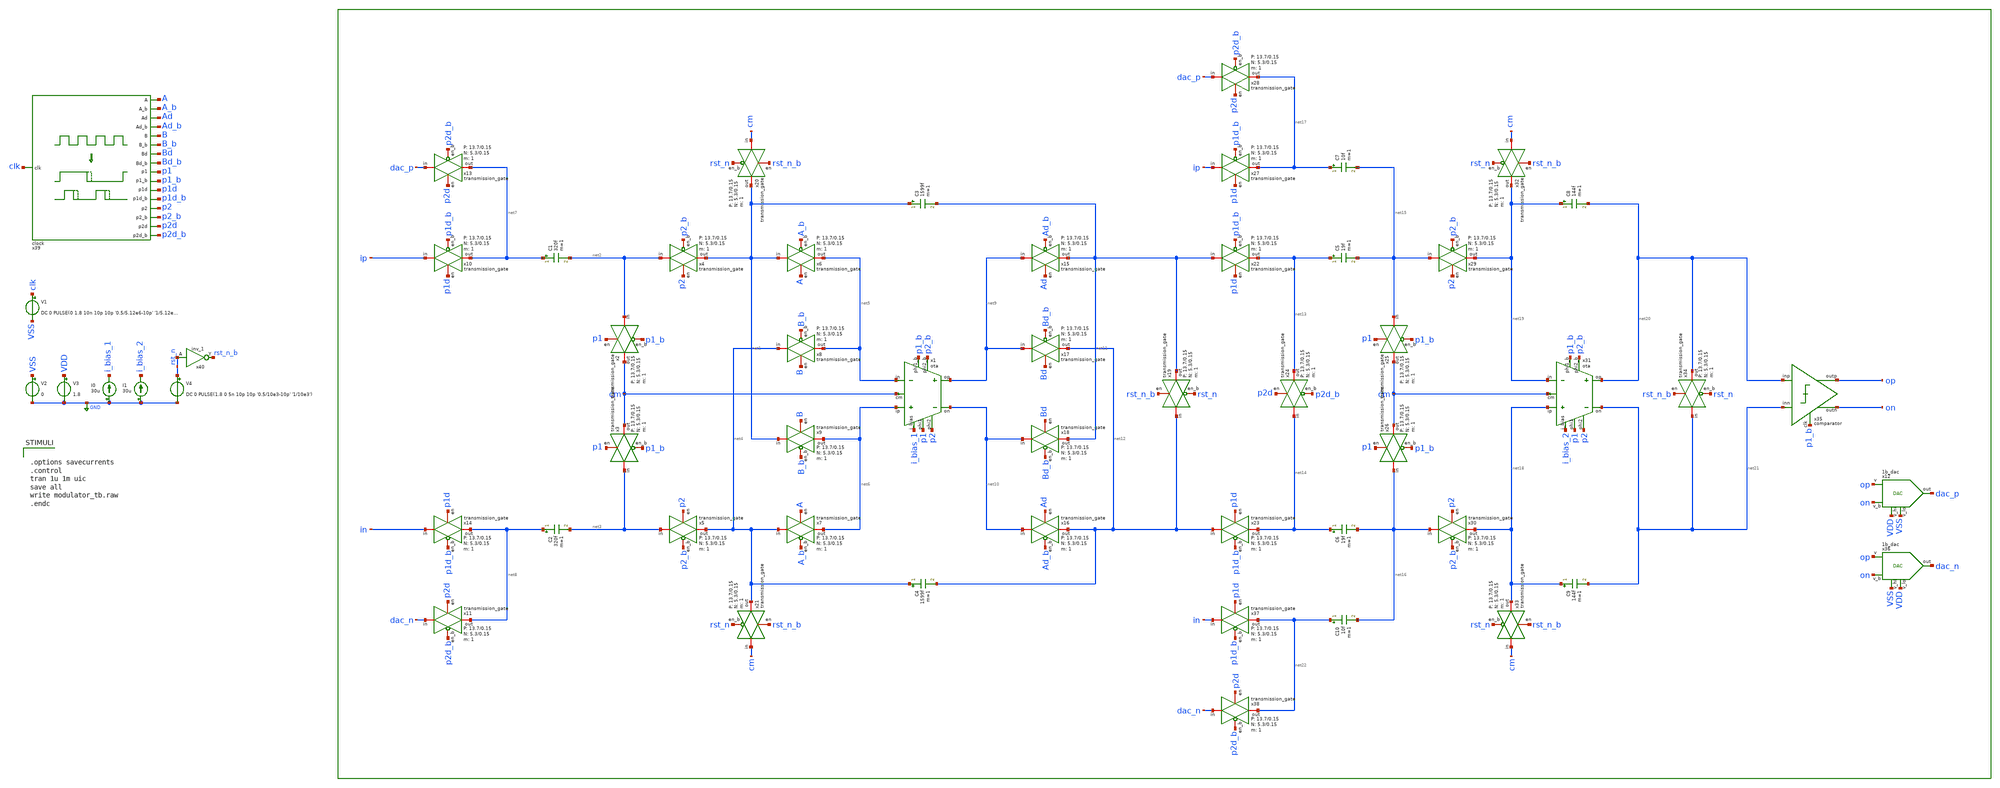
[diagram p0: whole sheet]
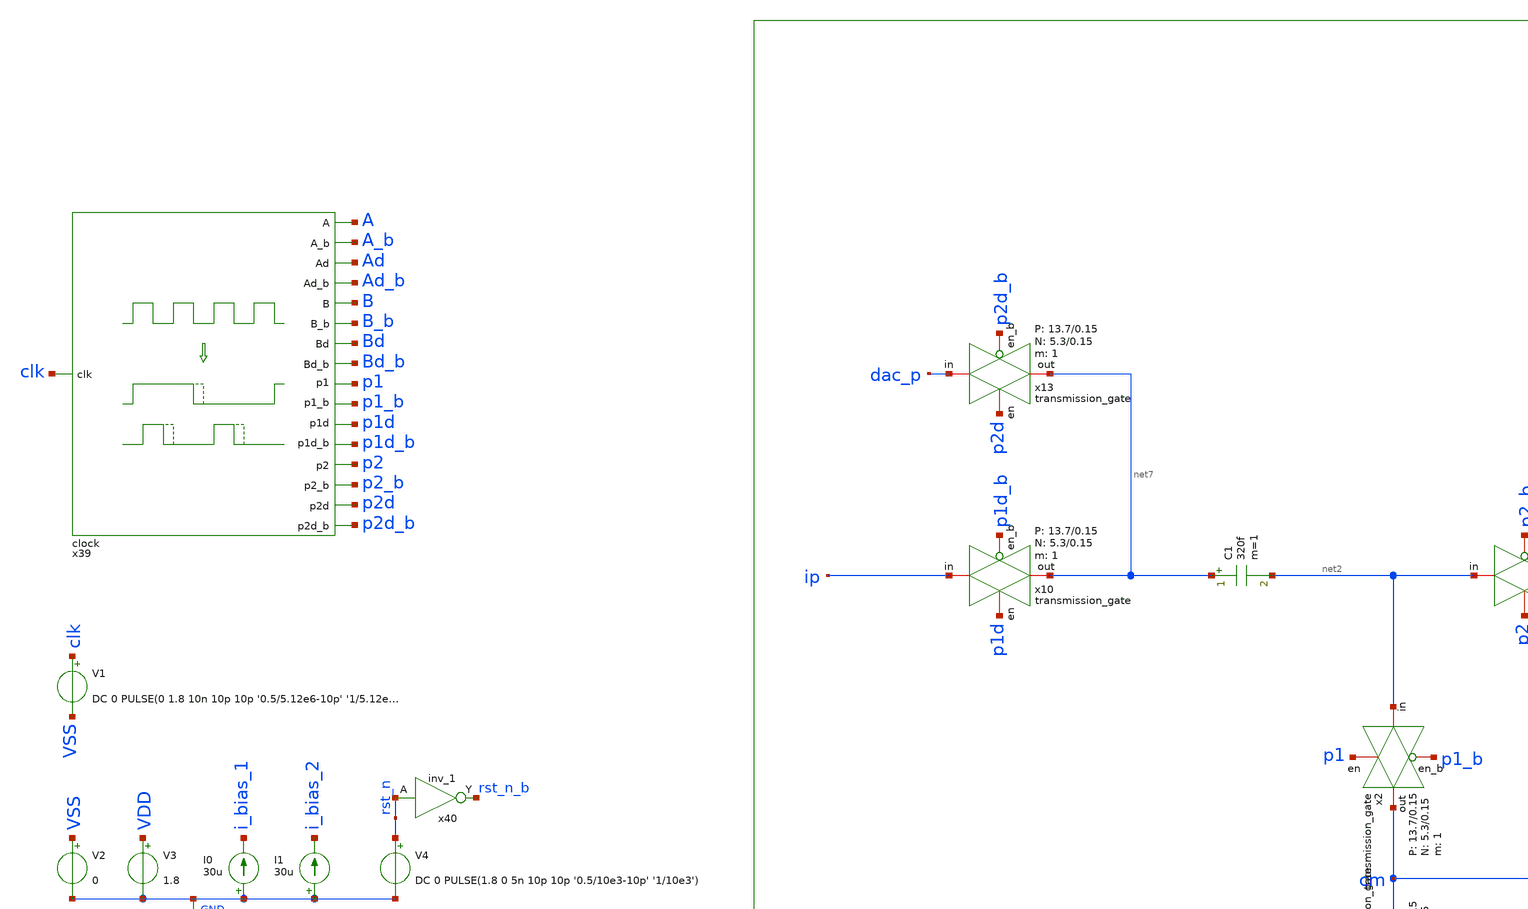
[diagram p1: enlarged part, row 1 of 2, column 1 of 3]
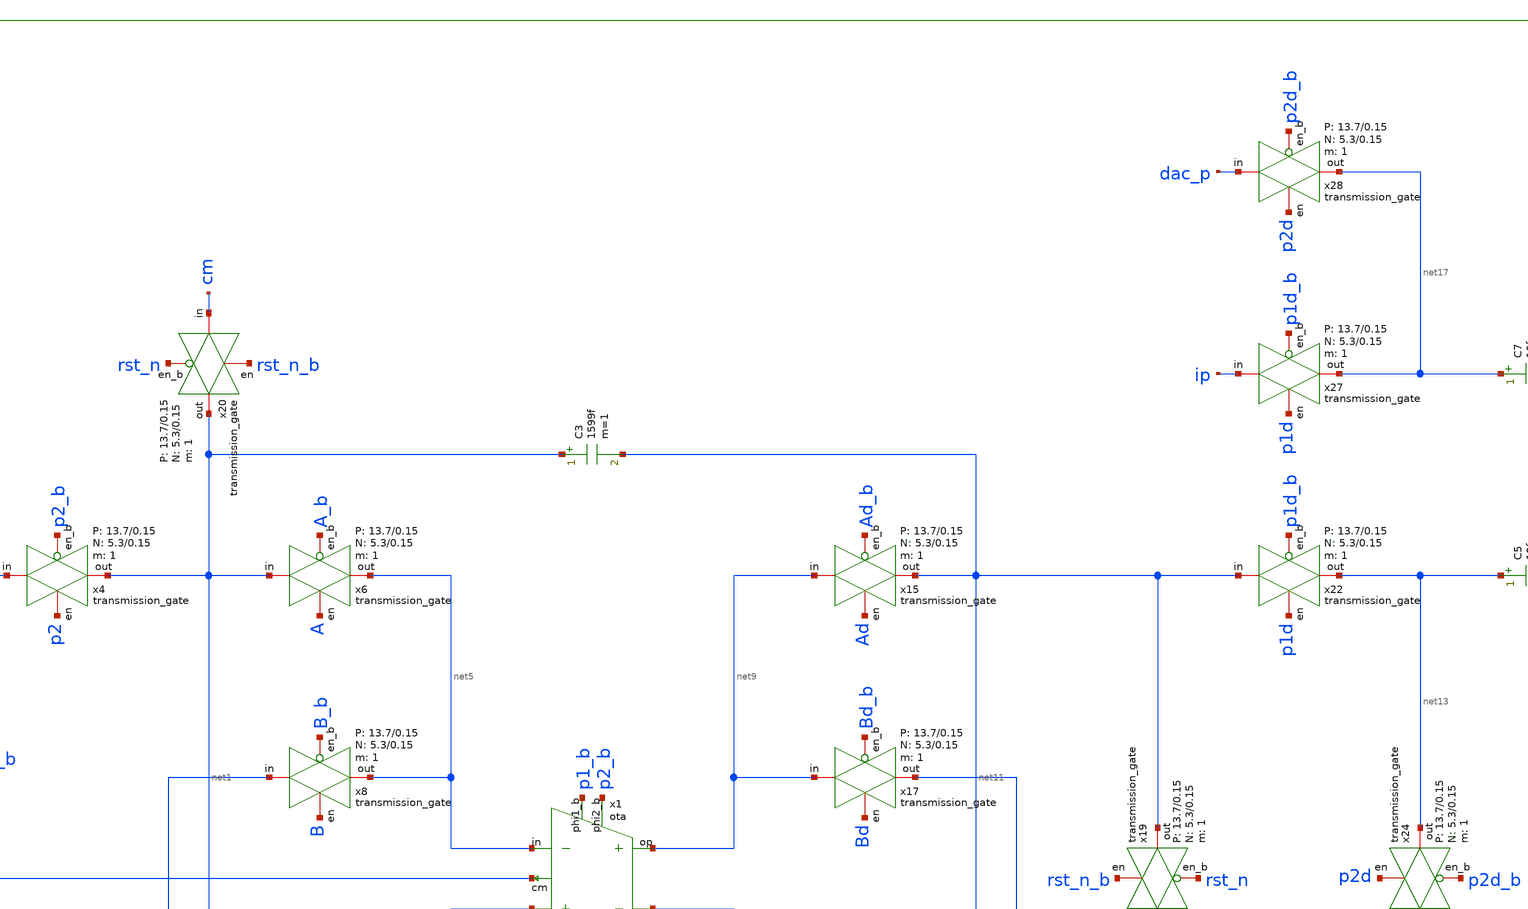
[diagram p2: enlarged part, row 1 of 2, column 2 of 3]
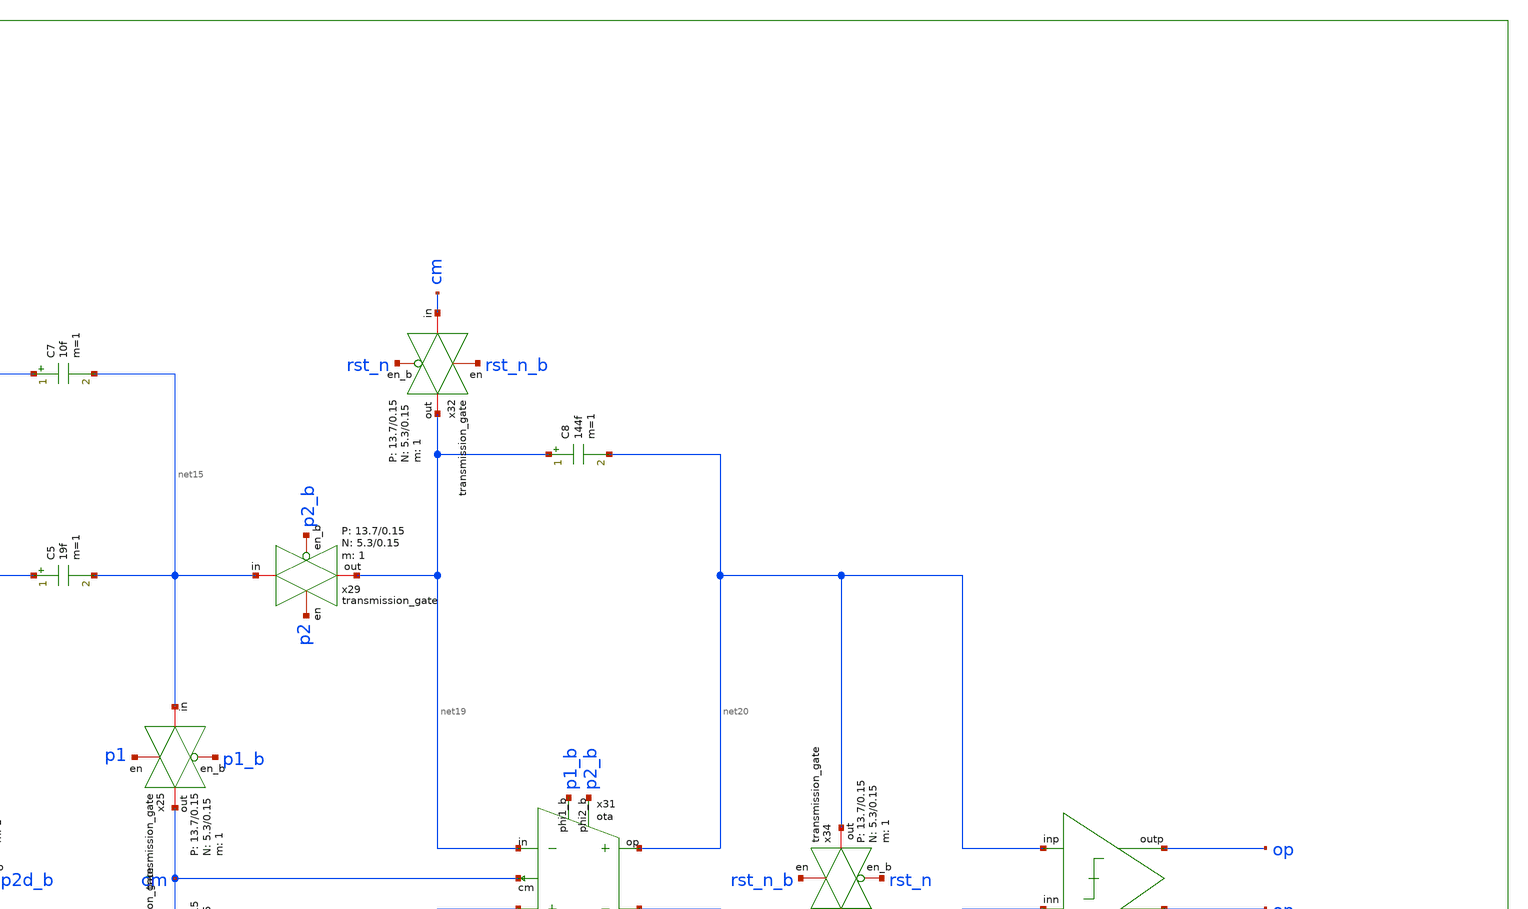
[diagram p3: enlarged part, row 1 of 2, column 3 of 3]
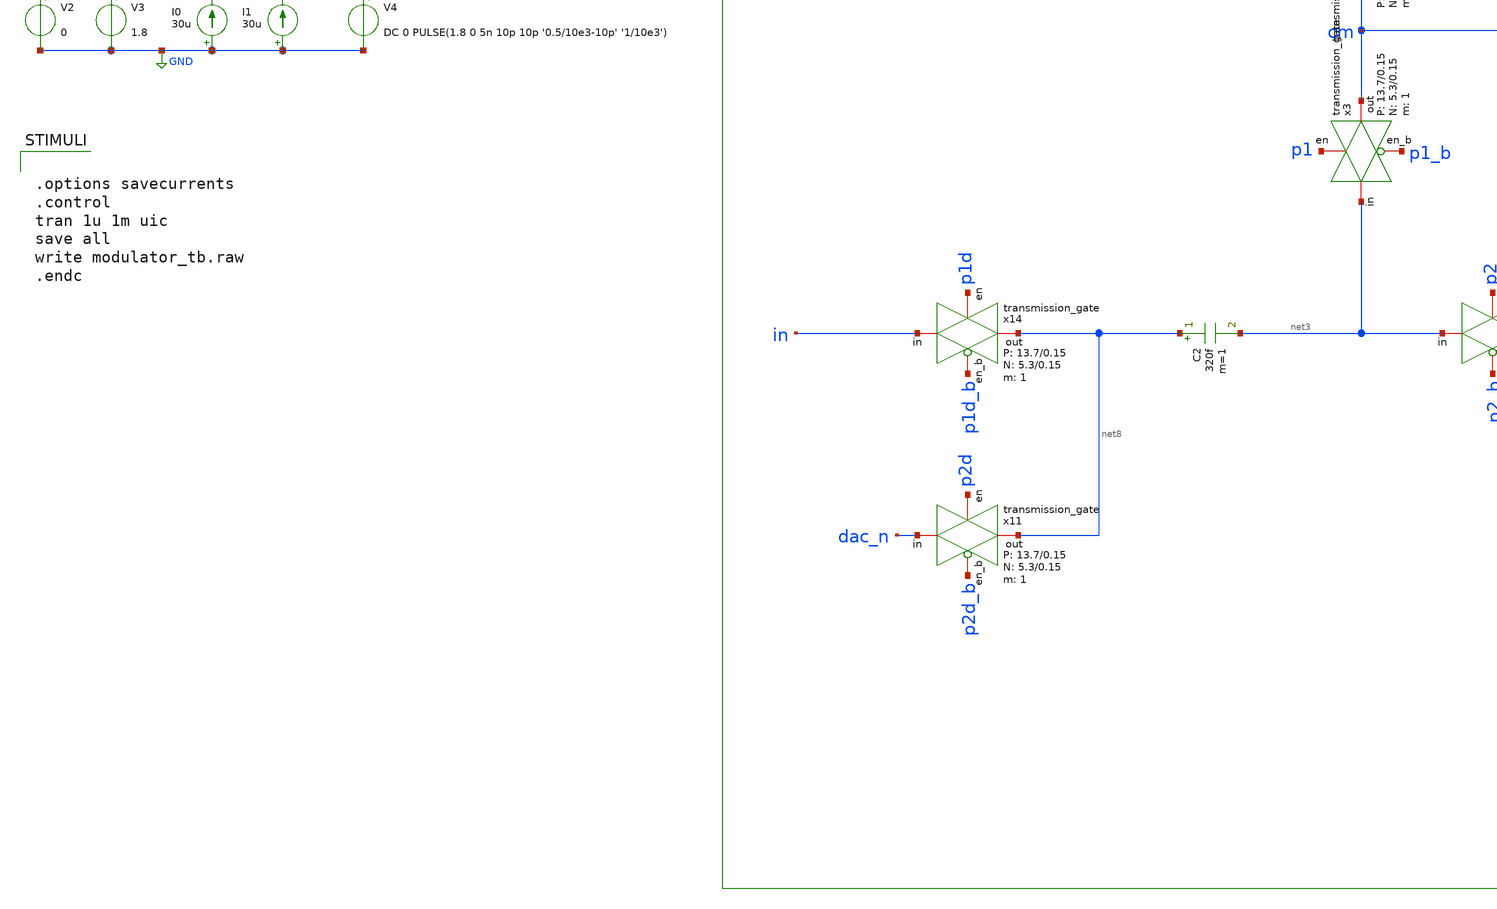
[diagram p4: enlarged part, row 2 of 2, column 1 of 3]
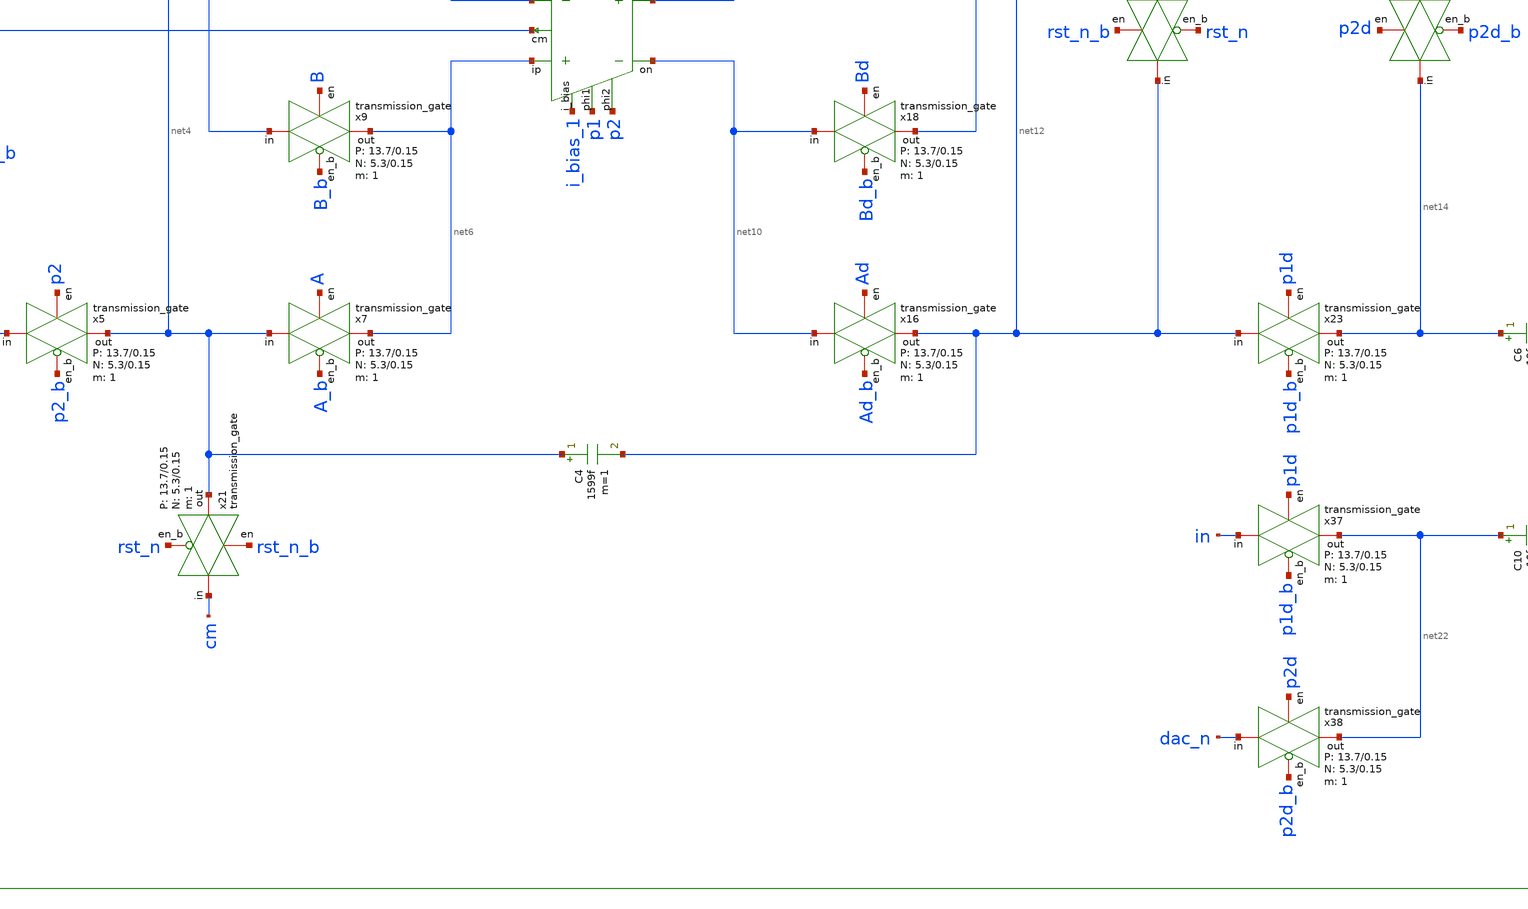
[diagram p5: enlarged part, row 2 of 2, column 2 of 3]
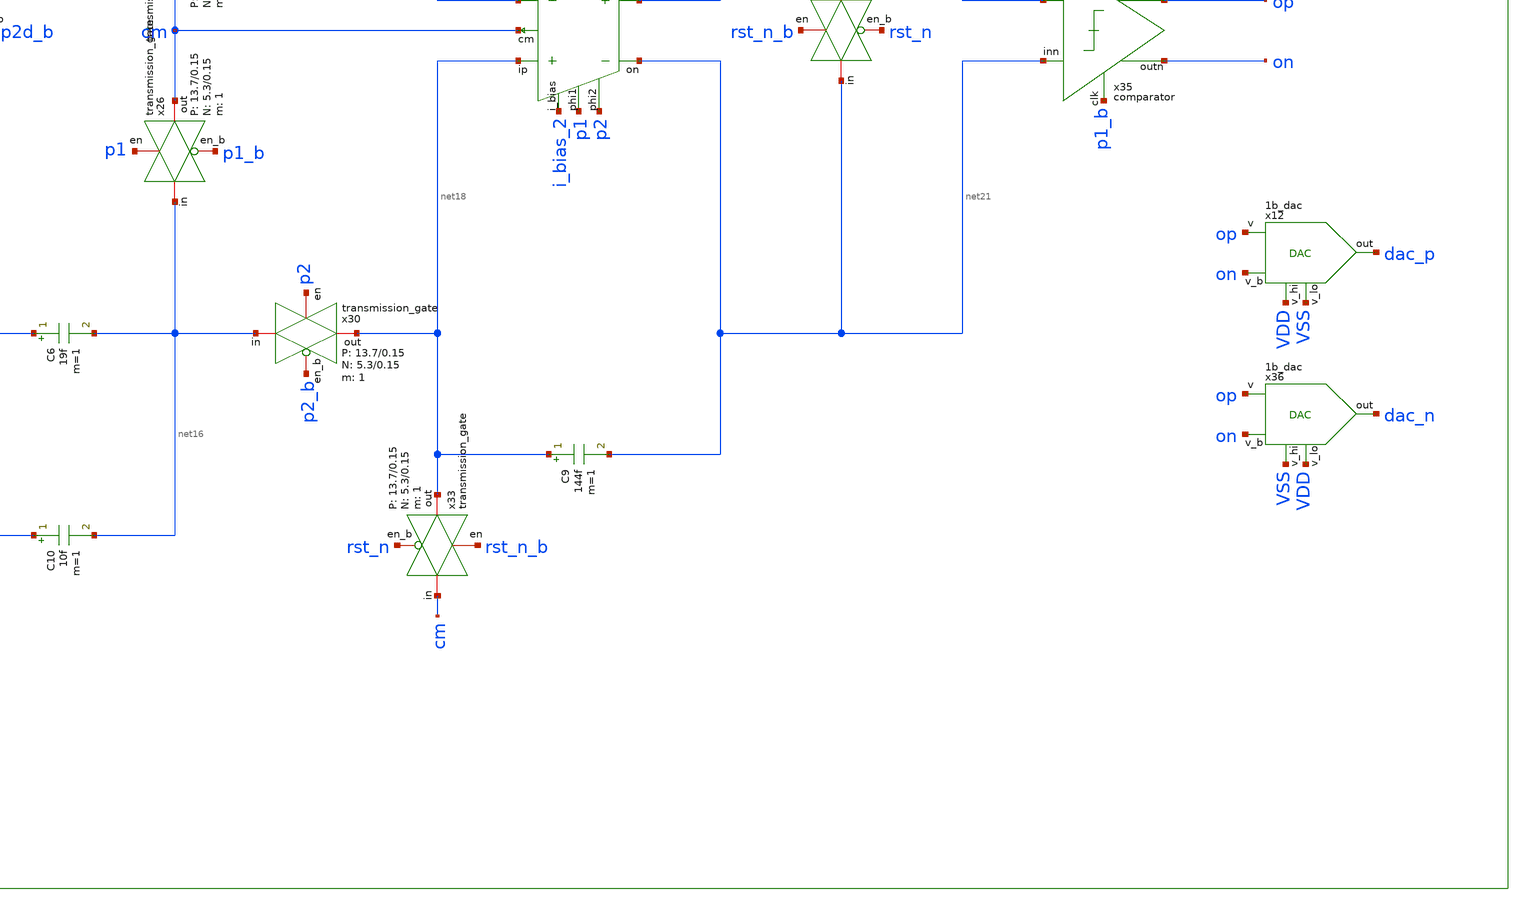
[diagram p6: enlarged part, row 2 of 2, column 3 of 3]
** sch_path: verification/schematic/modulator_tb.sch
**.subckt modulator_tb
x1 i_bias_1 net6 net5 p1 p1_b p2 p2_b net9 net10 cm 50 350 VDD VSS ota
x4 net2 net1 p2 p2_b VDD VSS 1 5.3 0.15 13.7 0.15 transmission_gate
x5 net3 net4 p2 p2_b VDD VSS 1 5.3 0.15 13.7 0.15 transmission_gate
x6 net1 net5 A A_b VDD VSS 1 5.3 0.15 13.7 0.15 transmission_gate
x7 net4 net6 A A_b VDD VSS 1 5.3 0.15 13.7 0.15 transmission_gate
x8 net4 net5 B B_b VDD VSS 1 5.3 0.15 13.7 0.15 transmission_gate
x9 net1 net6 B B_b VDD VSS 1 5.3 0.15 13.7 0.15 transmission_gate
x2 net2 cm p1 p1_b VDD VSS 1 5.3 0.15 13.7 0.15 transmission_gate
x3 net3 cm p1 p1_b VDD VSS 1 5.3 0.15 13.7 0.15 transmission_gate
C1 net7 net2 320f m=1
C2 net8 net3 320f m=1
x10 ip net7 p1d p1d_b VDD VSS 1 5.3 0.15 13.7 0.15 transmission_gate
x11 dac_n net8 p2d p2d_b VDD VSS 1 5.3 0.15 13.7 0.15 transmission_gate
x12 VDD VSS op dac_p on VDD VSS 1b_dac
x13 dac_p net7 p2d p2d_b VDD VSS 1 5.3 0.15 13.7 0.15 transmission_gate
x14 in net8 p1d p1d_b VDD VSS 1 5.3 0.15 13.7 0.15 transmission_gate
C3 net1 net11 1599f m=1
x15 net9 net11 Ad Ad_b VDD VSS 1 5.3 0.15 13.7 0.15 transmission_gate
x16 net10 net12 Ad Ad_b VDD VSS 1 5.3 0.15 13.7 0.15 transmission_gate
x17 net9 net12 Bd Bd_b VDD VSS 1 5.3 0.15 13.7 0.15 transmission_gate
x18 net10 net11 Bd Bd_b VDD VSS 1 5.3 0.15 13.7 0.15 transmission_gate
x19 net12 net11 rst_n_b rst_n VDD VSS 1 5.3 0.15 13.7 0.15 transmission_gate
C4 net4 net12 1599f m=1
x20 cm net1 rst_n_b rst_n VDD VSS 1 5.3 0.15 13.7 0.15 transmission_gate
x21 cm net4 rst_n_b rst_n VDD VSS 1 5.3 0.15 13.7 0.15 transmission_gate
x22 net11 net13 p1d p1d_b VDD VSS 1 5.3 0.15 13.7 0.15 transmission_gate
x23 net12 net14 p1d p1d_b VDD VSS 1 5.3 0.15 13.7 0.15 transmission_gate
x24 net14 net13 p2d p2d_b VDD VSS 1 5.3 0.15 13.7 0.15 transmission_gate
C5 net13 net15 19f m=1
C6 net14 net16 19f m=1
x25 net15 cm p1 p1_b VDD VSS 1 5.3 0.15 13.7 0.15 transmission_gate
x26 net16 cm p1 p1_b VDD VSS 1 5.3 0.15 13.7 0.15 transmission_gate
x27 ip net17 p1d p1d_b VDD VSS 1 5.3 0.15 13.7 0.15 transmission_gate
C7 net17 net15 10f m=1
x28 dac_p net17 p2d p2d_b VDD VSS 1 5.3 0.15 13.7 0.15 transmission_gate
x29 net15 net19 p2 p2_b VDD VSS 1 5.3 0.15 13.7 0.15 transmission_gate
x30 net16 net18 p2 p2_b VDD VSS 1 5.3 0.15 13.7 0.15 transmission_gate
x31 i_bias_2 net18 net19 p1 p1_b p2 p2_b net20 net21 cm 50 350 VDD VSS ota
x32 cm net19 rst_n_b rst_n VDD VSS 1 5.3 0.15 13.7 0.15 transmission_gate
C8 net19 net20 144f m=1
x33 cm net18 rst_n_b rst_n VDD VSS 1 5.3 0.15 13.7 0.15 transmission_gate
C9 net18 net21 144f m=1
x34 net21 net20 rst_n_b rst_n VDD VSS 1 5.3 0.15 13.7 0.15 transmission_gate
x35 net20 net21 op p1_b on VDD VSS comparator
x36 VSS VDD op dac_n on VDD VSS 1b_dac
x37 in net22 p1d p1d_b VDD VSS 1 5.3 0.15 13.7 0.15 transmission_gate
C10 net22 net16 10f m=1
x38 dac_n net22 p2d p2d_b VDD VSS 1 5.3 0.15 13.7 0.15 transmission_gate
x39 A A_b Ad Ad_b Bd_b Bd B_b B p2 p2_b p2d clk p2d_b p1d_b p1d p1_b p1 VDD VSS clock
V1 clk VSS DC 0 PULSE(0 1.8 10n 10p 10p '0.5/5.12e6-10p' '1/5.12e6')
V2 VSS GND 0
V3 VDD GND 1.8
I0 GND i_bias_1 30u
I1 GND i_bias_2 30u
V4 rst_n GND DC 0 PULSE(1.8 0 5n 10p 10p '0.5/10e3-10p' '1/10e3')
x40 rst_n VGND VNB VPB VPWR rst_n_b sky130_fd_sc_hd__inv_1
**** begin user architecture code

** opencircuitdesign pdks install
.lib /farmshare/home/classes/ee/372/PDKs/open_pdks_1.0.310/sky130/sky130A/libs.tech/ngspice/sky130.lib.spice tt
.inc /farmshare/home/classes/ee/372/PDKs/open_pdks_1.0.310/sky130/sky130A/libs.ref/sky130_fd_sc_hd/spice/sky130_fd_sc_hd.spice



.options savecurrents
.control
tran 1u 1m uic
save all
write modulator_tb.raw
.endc


**** end user architecture code
**.ends
.GLOBAL GND
.end
